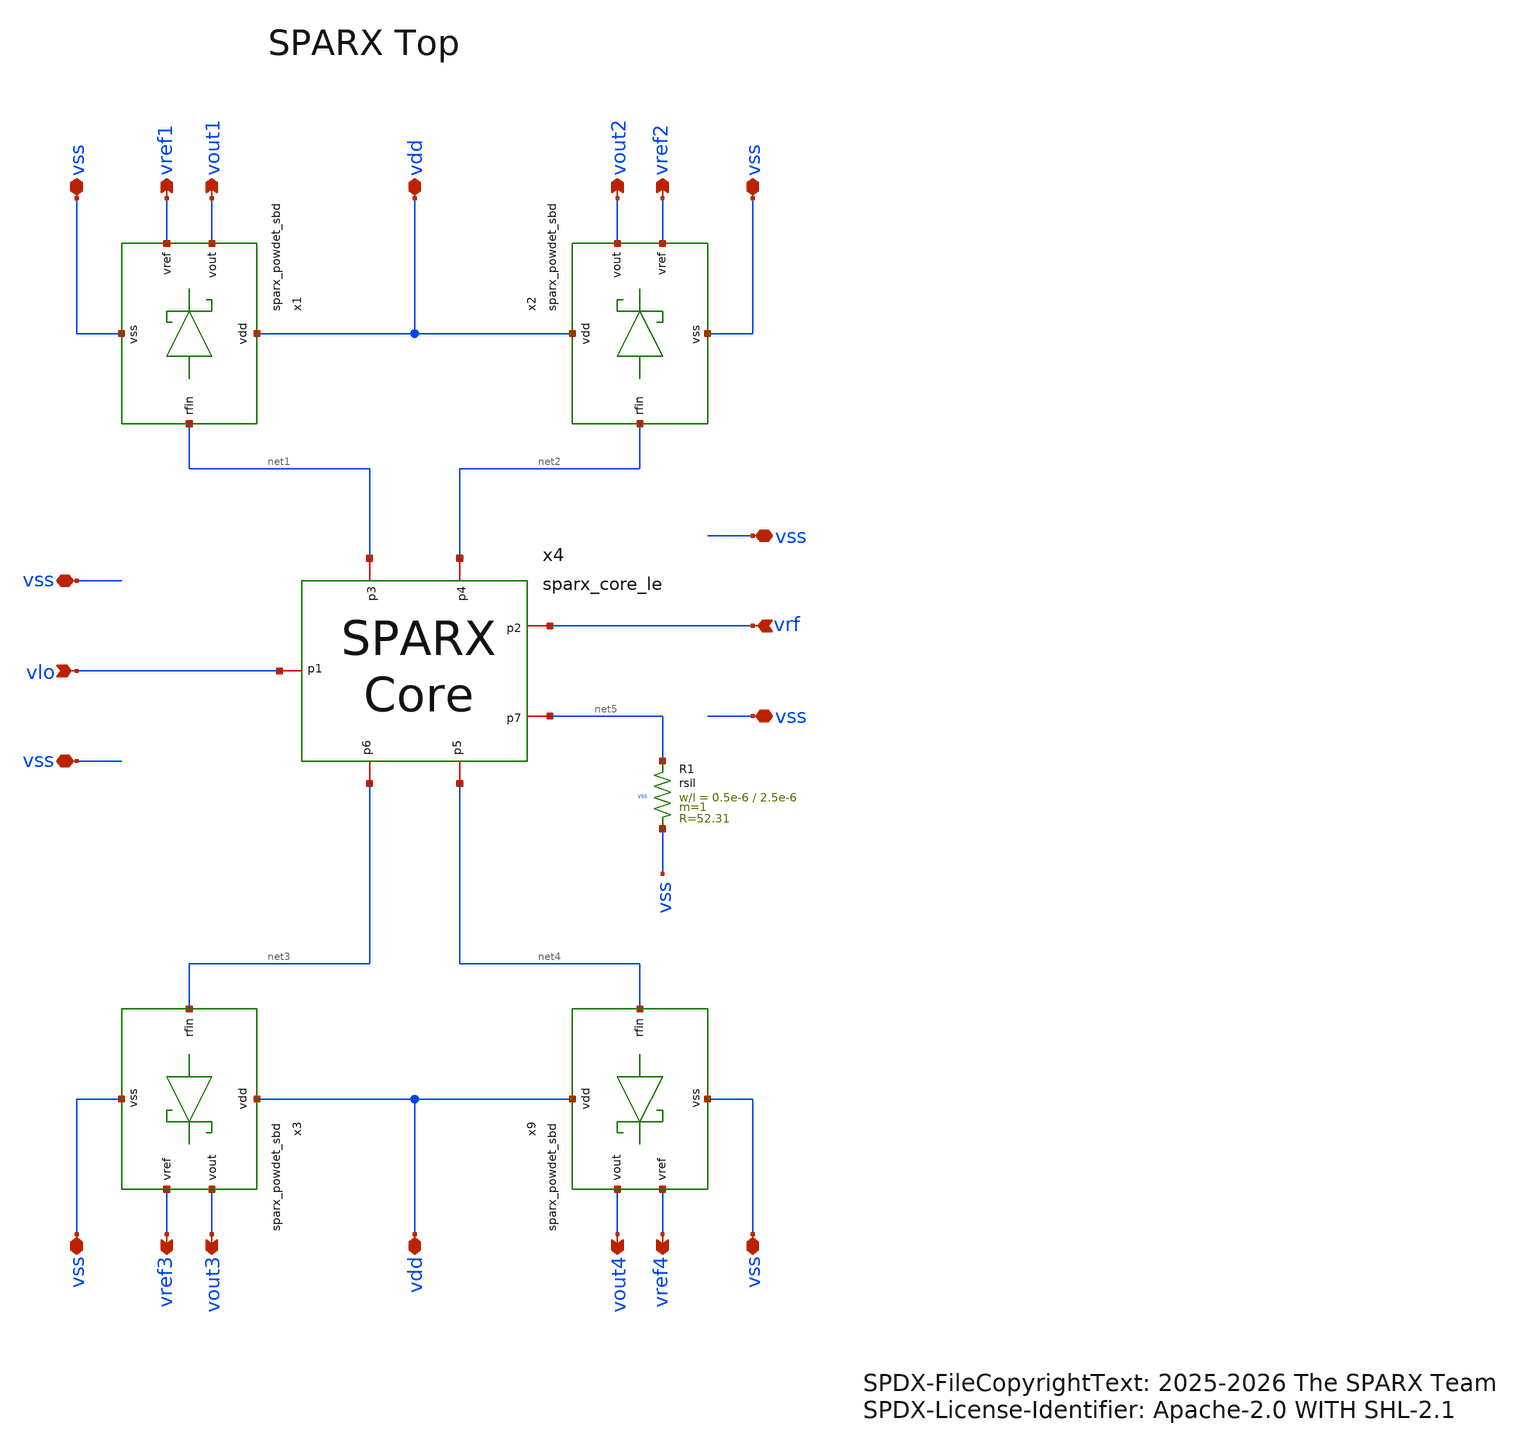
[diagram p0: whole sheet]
** sch_path: schematic/xschem/sparx_top_le.sch
* SPDX-FileCopyrightText: 2025-2026 The SPARX Team
* SPDX-License-Identifier: Apache-2.0 WITH SHL-2.1
**.subckt sparx_top_le vrf vout1 vdd vref1 vref2 vout2 vlo vss vss vout3 vdd vref3 vref4 vout4 vss
*+ vss vss vss vss vss
*.ipin vrf
*.opin vout1
*.iopin vdd
*.opin vref1
*.opin vref2
*.opin vout2
*.ipin vlo
*.iopin vss
*.iopin vss
*.opin vout3
*.iopin vdd
*.opin vref3
*.opin vref4
*.opin vout4
*.iopin vss
*.iopin vss
*.iopin vss
*.iopin vss
*.iopin vss
*.iopin vss
x1 vout1 vref1 vdd net1 vss sparx_powdet_sbd
x2 vout2 vref2 vdd net2 vss sparx_powdet_sbd
x3 vout3 vref3 vdd net3 vss sparx_powdet_sbd
x9 vout4 vref4 vdd net4 vss sparx_powdet_sbd
XR1 net5 vss vss rsil w=0.5e-6 l=2.5e-6 m=1 mm_ok=1
x4 vlo vrf net1 net2 net4 net3 net5 sparx_core_le
**.ends
.end
